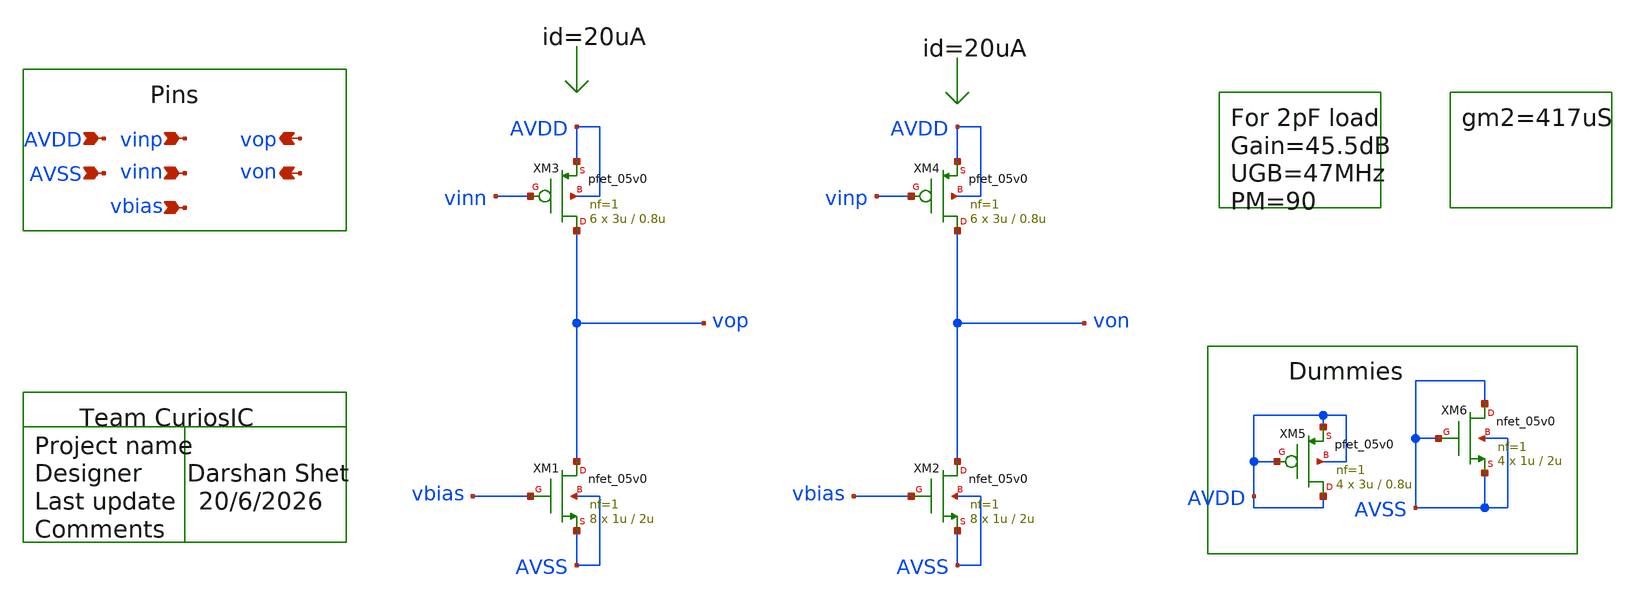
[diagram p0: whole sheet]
** sch_path: design/schematics/CCIA/Instrumentation Amplifier/DS_cic_bms_inst_amp_gm2.sch
**.subckt DS_cic_bms_inst_amp_gm2 vinp vinn von vop AVDD AVSS vbias
*.ipin vinp
*.ipin vinn
*.opin von
*.opin vop
*.ipin AVDD
*.ipin AVSS
*.ipin vbias
XM1 vop vbias AVSS AVSS nfet_05v0 L=2u W=1u nf=1 ad='int((nf+1)/2) * W/nf * 0.18u' as='int((nf+2)/2) * W/nf * 0.18u'
+ pd='2*int((nf+1)/2) * (W/nf + 0.18u)' ps='2*int((nf+2)/2) * (W/nf + 0.18u)' nrd='0.18u / W' nrs='0.18u / W'
+ sa=0 sb=0 sd=0 m=8
XM2 von vbias AVSS AVSS nfet_05v0 L=2u W=1u nf=1 ad='int((nf+1)/2) * W/nf * 0.18u' as='int((nf+2)/2) * W/nf * 0.18u'
+ pd='2*int((nf+1)/2) * (W/nf + 0.18u)' ps='2*int((nf+2)/2) * (W/nf + 0.18u)' nrd='0.18u / W' nrs='0.18u / W'
+ sa=0 sb=0 sd=0 m=8
XM3 vop vinn AVDD AVDD pfet_05v0 L=0.8u W=3u nf=1 ad='int((nf+1)/2) * W/nf * 0.18u' as='int((nf+2)/2) * W/nf * 0.18u'
+ pd='2*int((nf+1)/2) * (W/nf + 0.18u)' ps='2*int((nf+2)/2) * (W/nf + 0.18u)' nrd='0.18u / W' nrs='0.18u / W'
+ sa=0 sb=0 sd=0 m=6
XM4 von vinp AVDD AVDD pfet_05v0 L=0.8u W=3u nf=1 ad='int((nf+1)/2) * W/nf * 0.18u' as='int((nf+2)/2) * W/nf * 0.18u'
+ pd='2*int((nf+1)/2) * (W/nf + 0.18u)' ps='2*int((nf+2)/2) * (W/nf + 0.18u)' nrd='0.18u / W' nrs='0.18u / W'
+ sa=0 sb=0 sd=0 m=6
XM5 AVDD AVDD AVDD AVDD pfet_05v0 L=0.8u W=3u nf=1 ad='int((nf+1)/2) * W/nf * 0.18u' as='int((nf+2)/2) * W/nf * 0.18u'
+ pd='2*int((nf+1)/2) * (W/nf + 0.18u)' ps='2*int((nf+2)/2) * (W/nf + 0.18u)' nrd='0.18u / W' nrs='0.18u / W'
+ sa=0 sb=0 sd=0 m=4
XM6 AVSS AVSS AVSS AVSS nfet_05v0 L=2u W=1u nf=1 ad='int((nf+1)/2) * W/nf * 0.18u' as='int((nf+2)/2) * W/nf * 0.18u'
+ pd='2*int((nf+1)/2) * (W/nf + 0.18u)' ps='2*int((nf+2)/2) * (W/nf + 0.18u)' nrd='0.18u / W' nrs='0.18u / W'
+ sa=0 sb=0 sd=0 m=4
**.ends
.end
